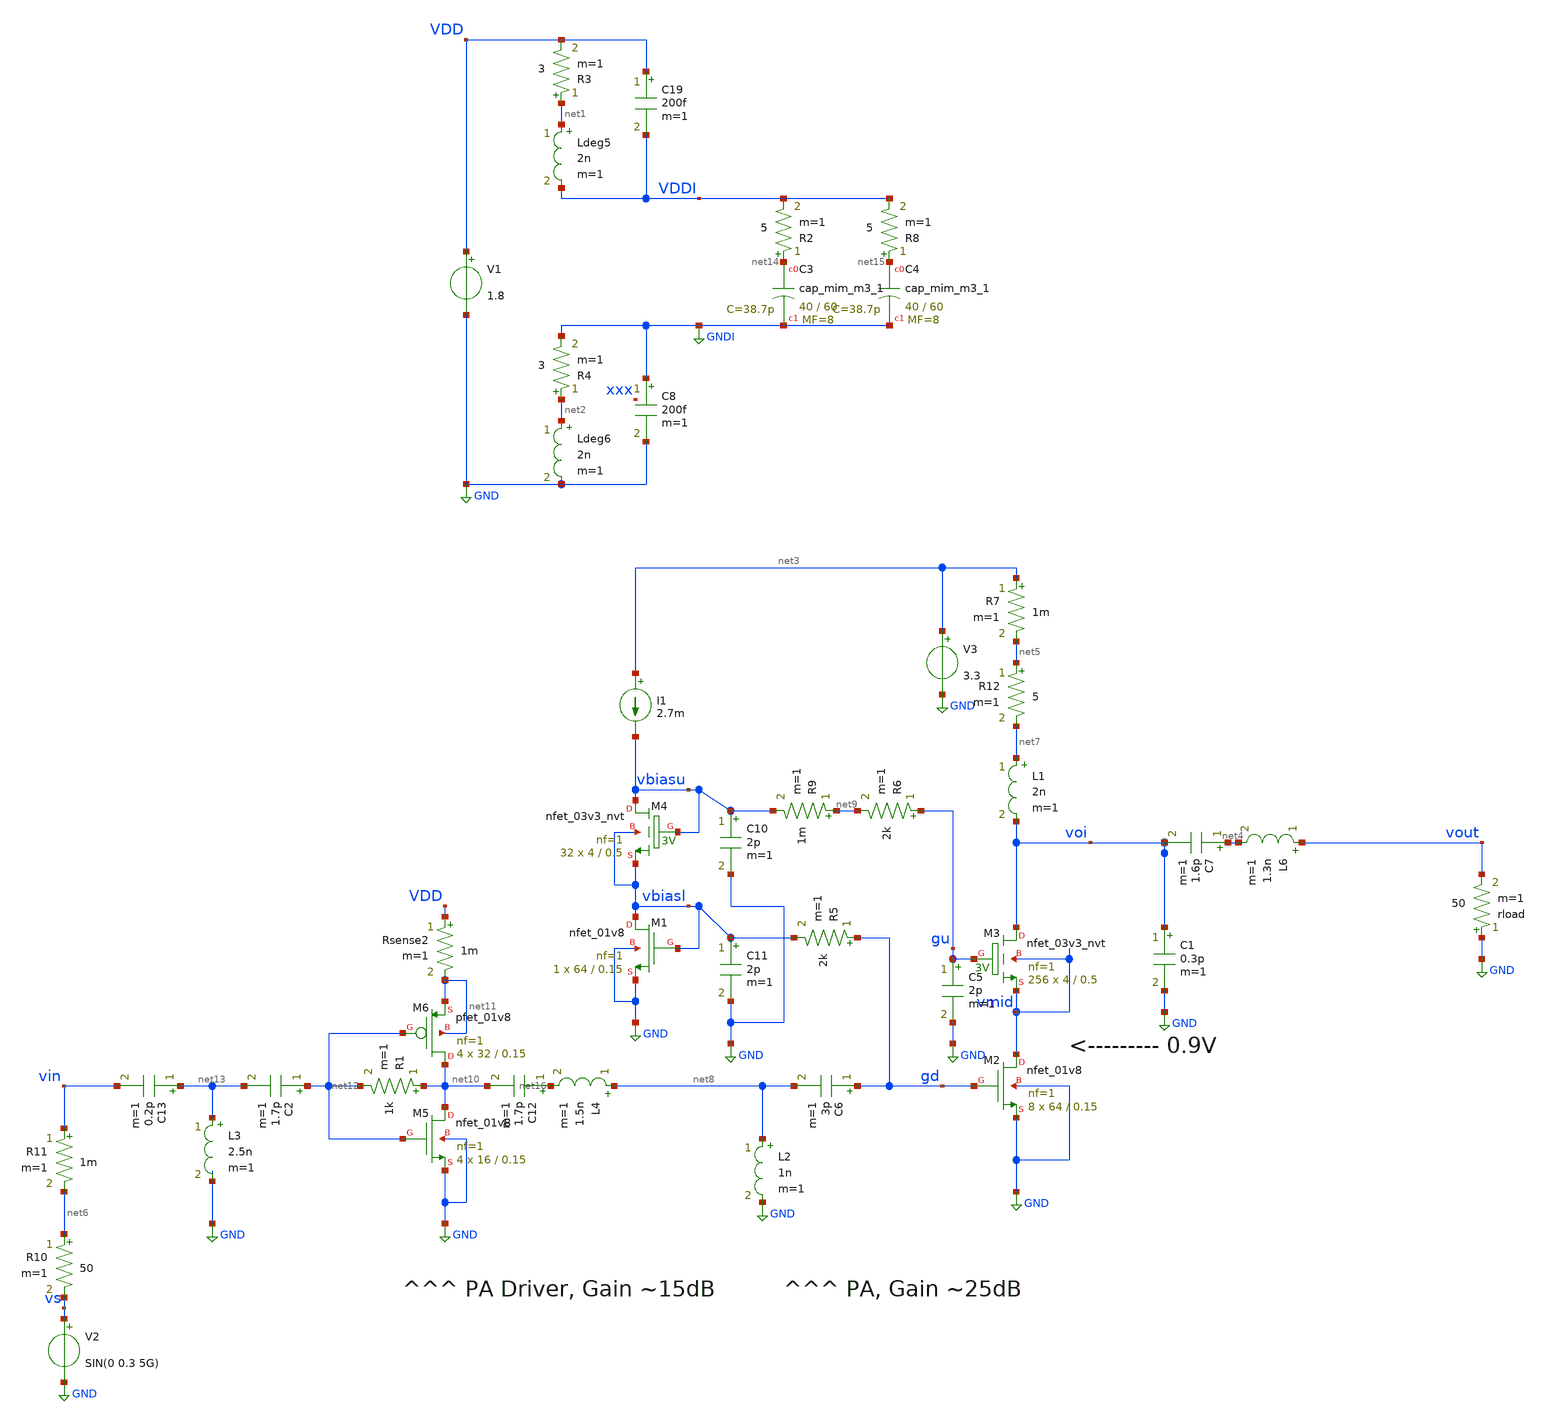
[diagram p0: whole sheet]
** sch_path: xschem/2stack_2.sch
**.subckt 2stack_2
V1 VDD GND 1.8
Ldeg5 net1 VDDI 2n m=1
R3 net1 VDD 3 m=1
Ldeg6 net2 GND 2n m=1
R4 net2 GNDI 3 m=1
XC3 net14 GNDI sky130_fd_pr__cap_mim_m3_1 W=40 L=60 MF=8 m=8
C8 GNDI GND 200f m=1
C19 VDD VDDI 200f m=1
R2 net14 VDDI 5 m=1
XC4 net15 GNDI sky130_fd_pr__cap_mim_m3_1 W=40 L=60 MF=8 m=8
R8 net15 VDDI 5 m=1
V2 vs GND SIN(0 0.3 5G)
V3 net3 GND 3.3
rload GND vout 50 m=1
L1 net7 voi 2n m=1
L6 vout net4 1.3n m=1
C7 net4 voi 1.6p m=1
C1 voi GND 0.3p m=1
R5 gd vbiasl 2k m=1
XM3 voi gu vmid vmid sky130_fd_pr__nfet_03v3_nvt L=0.5 W=4 nf=1 ad='int((nf+1)/2) * W/nf * 0.29' as='int((nf+2)/2) * W/nf * 0.29'
+ pd='2*int((nf+1)/2) * (W/nf + 0.29)' ps='2*int((nf+2)/2) * (W/nf + 0.29)' nrd='0.29 / W' nrs='0.29 / W'
+ sa=0 sb=0 sd=0 mult=256 m=256
R6 gu net9 2k m=1
C5 gu GND 2p m=1
R7 net3 net5 1m m=1
XM2 vmid gd GND GND sky130_fd_pr__nfet_01v8 L=0.15 W=64 nf=1 ad='int((nf+1)/2) * W/nf * 0.29' as='int((nf+2)/2) * W/nf * 0.29'
+ pd='2*int((nf+1)/2) * (W/nf + 0.29)' ps='2*int((nf+2)/2) * (W/nf + 0.29)' nrd='0.29 / W' nrs='0.29 / W'
+ sa=0 sb=0 sd=0 mult=8 m=8
R10 net6 vs 50 m=1
R11 vin net6 1m m=1
R12 net5 net7 5 m=1
C6 gd net8 3p m=1
L2 net8 GND 1n m=1
XM1 vbiasl vbiasl GND GND sky130_fd_pr__nfet_01v8 L=0.15 W=64 nf=1 ad='int((nf+1)/2) * W/nf * 0.29' as='int((nf+2)/2) * W/nf * 0.29'
+ pd='2*int((nf+1)/2) * (W/nf + 0.29)' ps='2*int((nf+2)/2) * (W/nf + 0.29)' nrd='0.29 / W' nrs='0.29 / W'
+ sa=0 sb=0 sd=0 mult=1 m=1
XM4 vbiasu vbiasu vbiasl vbiasl sky130_fd_pr__nfet_03v3_nvt L=0.5 W=4 nf=1 ad='int((nf+1)/2) * W/nf * 0.29'
+ as='int((nf+2)/2) * W/nf * 0.29' pd='2*int((nf+1)/2) * (W/nf + 0.29)' ps='2*int((nf+2)/2) * (W/nf + 0.29)'
+ nrd='0.29 / W' nrs='0.29 / W' sa=0 sb=0 sd=0 mult=32 m=32
I1 net3 vbiasu 2.7m
C10 vbiasu GND 2p m=1
C11 vbiasl GND 2p m=1
R9 net9 vbiasu 1m m=1
XM5 net10 net12 GND GND sky130_fd_pr__nfet_01v8 L=0.15 W=16 nf=1 ad='int((nf+1)/2) * W/nf * 0.29' as='int((nf+2)/2) * W/nf * 0.29'
+ pd='2*int((nf+1)/2) * (W/nf + 0.29)' ps='2*int((nf+2)/2) * (W/nf + 0.29)' nrd='0.29 / W' nrs='0.29 / W'
+ sa=0 sb=0 sd=0 mult=4 m=4
XM6 net10 net12 net11 net11 sky130_fd_pr__pfet_01v8 L=0.15 W=32 nf=1 ad='int((nf+1)/2) * W/nf * 0.29'
+ as='int((nf+2)/2) * W/nf * 0.29' pd='2*int((nf+1)/2) * (W/nf + 0.29)' ps='2*int((nf+2)/2) * (W/nf + 0.29)'
+ nrd='0.29 / W' nrs='0.29 / W' sa=0 sb=0 sd=0 mult=4 m=4
R1 net10 net12 1k m=1
C2 net12 net13 1.7p m=1
C12 net16 net10 1.7p m=1
C13 net13 vin 0.2p m=1
L3 net13 GND 2.5n m=1
L4 net8 net16 1.5n m=1
Rsense2 VDD net11 1m m=1
**** begin user architecture code
.lib $::SKYWATER_MODELS/sky130.lib.spice tt
* .include $::PDKPATH/libs.ref/sky130_fd_sc_hvl/spice/sky130_fd_sc_hvl.spice



.options savecurrents
* XMU_0 gu voi mid mid rf_nfet_6xaM02_extracted
* XMU_1 gu voi mid mid rf_nfet_6xaM02_extracted
* XMU_2 gu voi mid mid rf_nfet_6xaM02_extracted
* XMU_3 gu voi mid mid rf_nfet_6xaM02_extracted
* XMU_4 gu voi mid mid rf_nfet_6xaM02_extracted
* XMU_5 gu voi mid mid rf_nfet_6xaM02_extracted
* XMD_0 gd mid gnd gnd rf_nfet_6xaM02_extracted
* XMD_1 gd mid gnd gnd rf_nfet_6xaM02_extracted
* XMD_2 gd mid gnd gnd rf_nfet_6xaM02_extracted
* XMD_3 gd mid gnd gnd rf_nfet_6xaM02_extracted
* XMD_4 gd mid gnd gnd rf_nfet_6xaM02_extracted
* XMD_5 gd mid gnd gnd rf_nfet_6xaM02_extracted
.tran 5ps 20ns

.control
run
display
plot @r5[i]
let zout=@rload[r]
let zin=50
meas TRAN vout_rms rms v(vout)

meas TRAN isp_hi_avg  avg @r7[i]
meas TRAN isp_mid_avg avg @r9[i]
meas TRAN vin_rms rms v(vin)
meas TRAN isp_1p8_avg avg @rsense2[i]


let psp_rms  = isp_hi_avg*3.6 + isp_mid_avg*2.2 + isp_1p8_avg * 1.8
let pout_rms = vout_rms^2/zout
let pin_rms  = vin_rms^2/zin
print psp_rms
print ((pout_rms-pin_rms)/psp_rms)*100
print 10*log10(pout_rms*1000)

plot gd vmid voi vout

* let pout = mag(@rload[i]*vout)
* let poutdbm = log10((pout/(1e-3))*10
* plot pout


* For the safty of the 3v3 transistor...
let vdsu = voi-vmid
let vgsu = gu-vmid
let vgdu = voi-gu
plot vdsu
plot vgsu
plot vgdu
* let vgbu = gu-vmid * the same as

.endc


**** end user architecture code
**.ends
.GLOBAL GND
.GLOBAL GNDI
.end
